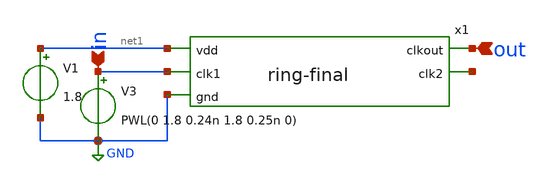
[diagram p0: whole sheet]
** sch_path: week4/xschem/analog_onlyring_tb.sch
**.subckt analog_onlyring_tb out in
*.ipin out
*.ipin in
x1 net1 out in net2 GND ring-final
V1 net1 GND 1.8
V3 in GND PWL(0 1.8 0.24n 1.8 0.25n 0)
**** begin user architecture code


.lib /usr/local/share/pdk/sky130A/libs.tech/ngspice/sky130.lib.spice tt
.control
	tran 0.01n 4n
	plot v(in) v(out)
.endc
.save all


**** end user architecture code
**.ends

* expanding   symbol:  ring-final.sym # of pins=5
** sym_path: week4/xschem/ring-final.sym
** sch_path: week4/xschem/ring-final.sch
.subckt ring-final vdd clkout clk1 clk2 gnd
*.ipin vdd
*.ipin gnd
*.ipin clk1
*.opin clkout
*.opin clk2
XM7 vdd clk1 clkin gnd sky130_fd_pr__nfet_01v8 L=0.15 W=1 nf=1 ad='int((nf+1)/2) * W/nf * 0.29' as='int((nf+2)/2) * W/nf * 0.29'
+ pd='2*int((nf+1)/2) * (W/nf + 0.29)' ps='2*int((nf+2)/2) * (W/nf + 0.29)' nrd='0.29 / W' nrs='0.29 / W'
+ sa=0 sb=0 sd=0 mult=1 m=1
XM8 clk2 clk1 gnd gnd sky130_fd_pr__nfet_01v8 L=0.15 W=1 nf=1 ad='int((nf+1)/2) * W/nf * 0.29' as='int((nf+2)/2) * W/nf * 0.29'
+ pd='2*int((nf+1)/2) * (W/nf + 0.29)' ps='2*int((nf+2)/2) * (W/nf + 0.29)' nrd='0.29 / W' nrs='0.29 / W'
+ sa=0 sb=0 sd=0 mult=1 m=1
XM9 clk2 clk1 vdd vdd sky130_fd_pr__pfet_01v8 L=0.15 W=1 nf=1 ad='int((nf+1)/2) * W/nf * 0.29' as='int((nf+2)/2) * W/nf * 0.29'
+ pd='2*int((nf+1)/2) * (W/nf + 0.29)' ps='2*int((nf+2)/2) * (W/nf + 0.29)' nrd='0.29 / W' nrs='0.29 / W'
+ sa=0 sb=0 sd=0 mult=1 m=1
XM10 clkout clk2 clkin gnd sky130_fd_pr__nfet_01v8 L=0.15 W=1 nf=1 ad='int((nf+1)/2) * W/nf * 0.29' as='int((nf+2)/2) * W/nf * 0.29'
+ pd='2*int((nf+1)/2) * (W/nf + 0.29)' ps='2*int((nf+2)/2) * (W/nf + 0.29)' nrd='0.29 / W' nrs='0.29 / W'
+ sa=0 sb=0 sd=0 mult=1 m=1
XM1 net1 clkin gnd gnd sky130_fd_pr__nfet_01v8 L=0.15 W=1 nf=1 ad='int((nf+1)/2) * W/nf * 0.29' as='int((nf+2)/2) * W/nf * 0.29'
+ pd='2*int((nf+1)/2) * (W/nf + 0.29)' ps='2*int((nf+2)/2) * (W/nf + 0.29)' nrd='0.29 / W' nrs='0.29 / W'
+ sa=0 sb=0 sd=0 mult=1 m=1
XM2 net1 clkin vdd vdd sky130_fd_pr__pfet_01v8 L=0.15 W=3 nf=1 ad='int((nf+1)/2) * W/nf * 0.29' as='int((nf+2)/2) * W/nf * 0.29'
+ pd='2*int((nf+1)/2) * (W/nf + 0.29)' ps='2*int((nf+2)/2) * (W/nf + 0.29)' nrd='0.29 / W' nrs='0.29 / W'
+ sa=0 sb=0 sd=0 mult=1 m=1
XM3 net2 net1 gnd gnd sky130_fd_pr__nfet_01v8 L=0.15 W=1 nf=1 ad='int((nf+1)/2) * W/nf * 0.29' as='int((nf+2)/2) * W/nf * 0.29'
+ pd='2*int((nf+1)/2) * (W/nf + 0.29)' ps='2*int((nf+2)/2) * (W/nf + 0.29)' nrd='0.29 / W' nrs='0.29 / W'
+ sa=0 sb=0 sd=0 mult=1 m=1
XM4 net2 net1 vdd vdd sky130_fd_pr__pfet_01v8 L=0.15 W=6 nf=1 ad='int((nf+1)/2) * W/nf * 0.29' as='int((nf+2)/2) * W/nf * 0.29'
+ pd='2*int((nf+1)/2) * (W/nf + 0.29)' ps='2*int((nf+2)/2) * (W/nf + 0.29)' nrd='0.29 / W' nrs='0.29 / W'
+ sa=0 sb=0 sd=0 mult=1 m=1
XM5 clkout net3 gnd gnd sky130_fd_pr__nfet_01v8 L=0.15 W=1 nf=1 ad='int((nf+1)/2) * W/nf * 0.29' as='int((nf+2)/2) * W/nf * 0.29'
+ pd='2*int((nf+1)/2) * (W/nf + 0.29)' ps='2*int((nf+2)/2) * (W/nf + 0.29)' nrd='0.29 / W' nrs='0.29 / W'
+ sa=0 sb=0 sd=0 mult=1 m=1
XM6 clkout net3 vdd vdd sky130_fd_pr__pfet_01v8 L=0.15 W=48 nf=1 ad='int((nf+1)/2) * W/nf * 0.29' as='int((nf+2)/2) * W/nf * 0.29'
+ pd='2*int((nf+1)/2) * (W/nf + 0.29)' ps='2*int((nf+2)/2) * (W/nf + 0.29)' nrd='0.29 / W' nrs='0.29 / W'
+ sa=0 sb=0 sd=0 mult=1 m=1
XM11 net4 net2 gnd gnd sky130_fd_pr__nfet_01v8 L=0.15 W=1 nf=1 ad='int((nf+1)/2) * W/nf * 0.29' as='int((nf+2)/2) * W/nf * 0.29'
+ pd='2*int((nf+1)/2) * (W/nf + 0.29)' ps='2*int((nf+2)/2) * (W/nf + 0.29)' nrd='0.29 / W' nrs='0.29 / W'
+ sa=0 sb=0 sd=0 mult=1 m=1
XM12 net4 net2 vdd vdd sky130_fd_pr__pfet_01v8 L=0.15 W=12 nf=1 ad='int((nf+1)/2) * W/nf * 0.29' as='int((nf+2)/2) * W/nf * 0.29'
+ pd='2*int((nf+1)/2) * (W/nf + 0.29)' ps='2*int((nf+2)/2) * (W/nf + 0.29)' nrd='0.29 / W' nrs='0.29 / W'
+ sa=0 sb=0 sd=0 mult=1 m=1
XM13 net3 net4 gnd gnd sky130_fd_pr__nfet_01v8 L=0.15 W=1 nf=1 ad='int((nf+1)/2) * W/nf * 0.29' as='int((nf+2)/2) * W/nf * 0.29'
+ pd='2*int((nf+1)/2) * (W/nf + 0.29)' ps='2*int((nf+2)/2) * (W/nf + 0.29)' nrd='0.29 / W' nrs='0.29 / W'
+ sa=0 sb=0 sd=0 mult=1 m=1
XM14 net3 net4 vdd vdd sky130_fd_pr__pfet_01v8 L=0.15 W=24 nf=1 ad='int((nf+1)/2) * W/nf * 0.29' as='int((nf+2)/2) * W/nf * 0.29'
+ pd='2*int((nf+1)/2) * (W/nf + 0.29)' ps='2*int((nf+2)/2) * (W/nf + 0.29)' nrd='0.29 / W' nrs='0.29 / W'
+ sa=0 sb=0 sd=0 mult=1 m=1
.ends

.GLOBAL GND
.end
